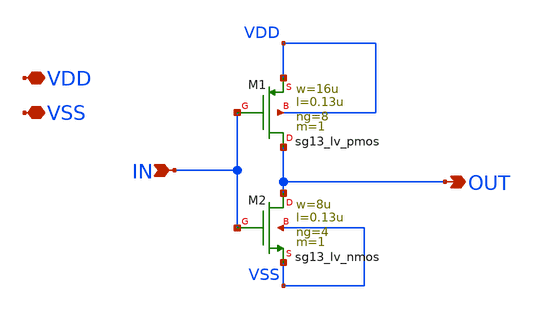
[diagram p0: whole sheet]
** sch_path: xschem/single_inverter.sch
**.subckt single_inverter VDD VSS IN OUT
*.iopin VDD
*.iopin VSS
*.ipin IN
*.opin OUT
XM1 OUT IN VDD VDD sg13_lv_pmos w=16u l=0.13u ng=8 m=1 mm_ok=1
XM2 OUT IN VSS VSS sg13_lv_nmos w=8u l=0.13u ng=4 m=1 mm_ok=1
**.ends
.end
